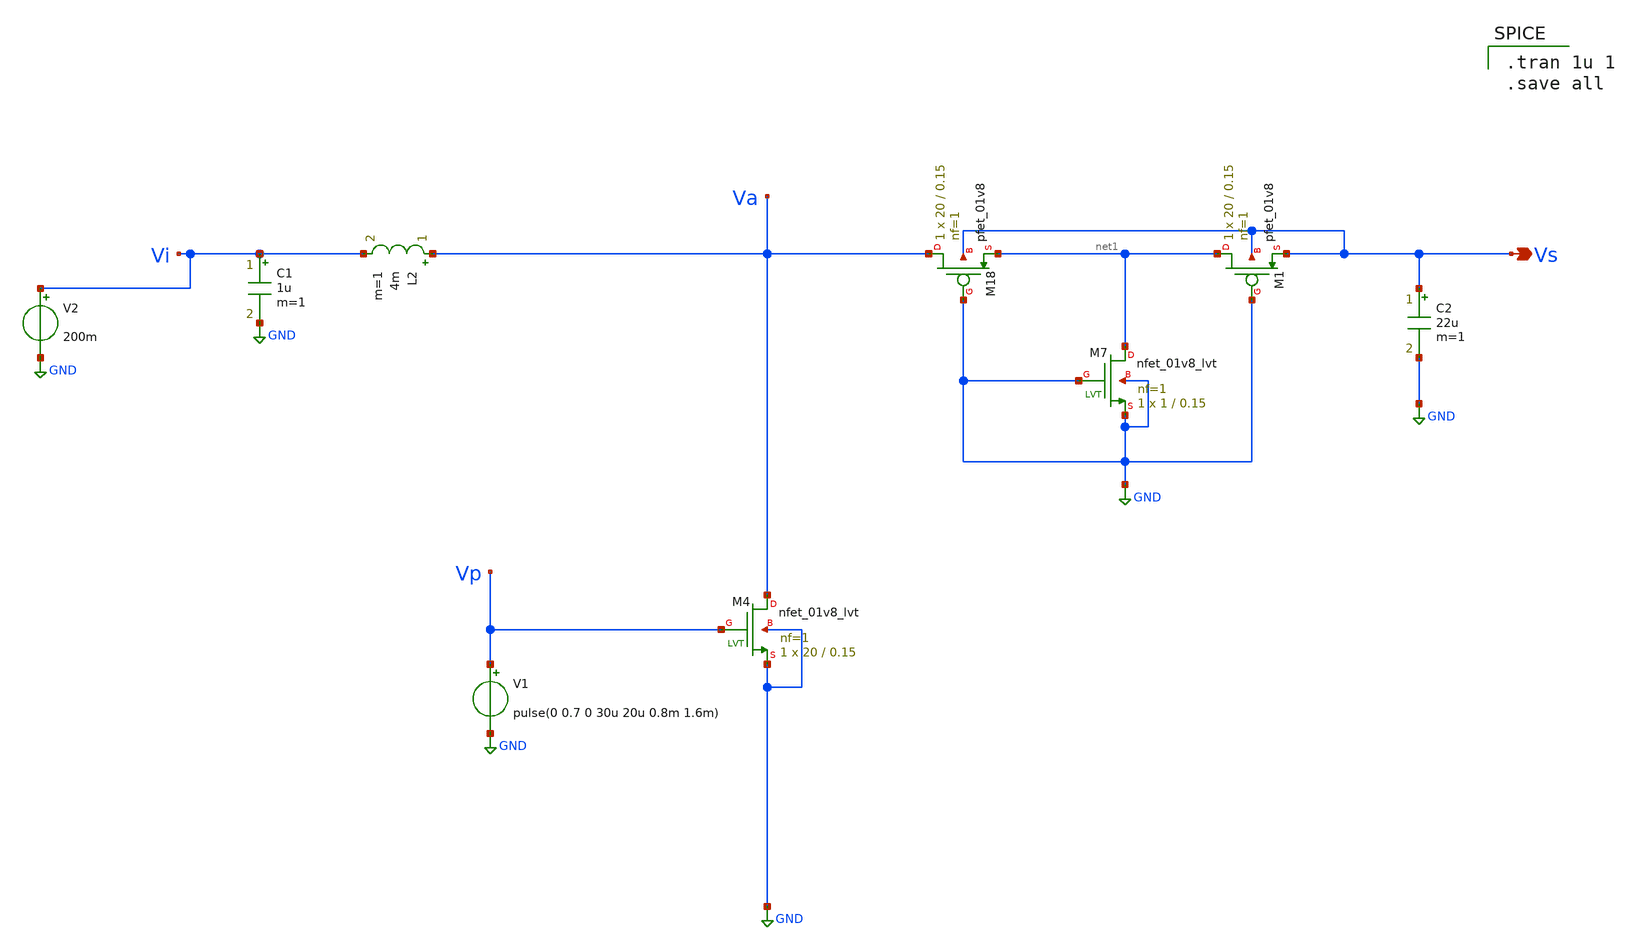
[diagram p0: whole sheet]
** sch_path: Blocks/Startup Converter/test_1.sch
**.subckt test_1 Vs
*.opin Vs
C1 Vi GND 1u m=1
L2 Va Vi 4m m=1
C2 Vs GND 22u m=1
XM4 Va Vp GND GND sky130_fd_pr__nfet_01v8_lvt L=0.15 W=20 nf=1 ad='int((nf+1)/2) * W/nf * 0.29' as='int((nf+2)/2) * W/nf * 0.29'
+ pd='2*int((nf+1)/2) * (W/nf + 0.29)' ps='2*int((nf+2)/2) * (W/nf + 0.29)' nrd='0.29 / W' nrs='0.29 / W'
+ sa=0 sb=0 sd=0 mult=1 m=1
XM7 net1 GND GND GND sky130_fd_pr__nfet_01v8_lvt L=0.15 W=1 nf=1 ad='int((nf+1)/2) * W/nf * 0.29' as='int((nf+2)/2) * W/nf * 0.29'
+ pd='2*int((nf+1)/2) * (W/nf + 0.29)' ps='2*int((nf+2)/2) * (W/nf + 0.29)' nrd='0.29 / W' nrs='0.29 / W'
+ sa=0 sb=0 sd=0 mult=1 m=1
V1 Vp GND pulse(0 0.7 0 30u 20u 0.8m 1.6m)
V2 Vi GND 200m
XM18 Va GND net1 Vs sky130_fd_pr__pfet_01v8 L=0.15 W=20 nf=1 ad='int((nf+1)/2) * W/nf * 0.29' as='int((nf+2)/2) * W/nf * 0.29'
+ pd='2*int((nf+1)/2) * (W/nf + 0.29)' ps='2*int((nf+2)/2) * (W/nf + 0.29)' nrd='0.29 / W' nrs='0.29 / W'
+ sa=0 sb=0 sd=0 mult=1 m=1
XM1 net1 GND Vs Vs sky130_fd_pr__pfet_01v8 L=0.15 W=20 nf=1 ad='int((nf+1)/2) * W/nf * 0.29' as='int((nf+2)/2) * W/nf * 0.29'
+ pd='2*int((nf+1)/2) * (W/nf + 0.29)' ps='2*int((nf+2)/2) * (W/nf + 0.29)' nrd='0.29 / W' nrs='0.29 / W'
+ sa=0 sb=0 sd=0 mult=1 m=1
**** begin user architecture code

** opencircuitdesign pdks install
.lib $::SKYWATER_MODELS/sky130.lib.spice tt



.tran 1u 1
.save all

**** end user architecture code
**.ends
.GLOBAL GND
.end
